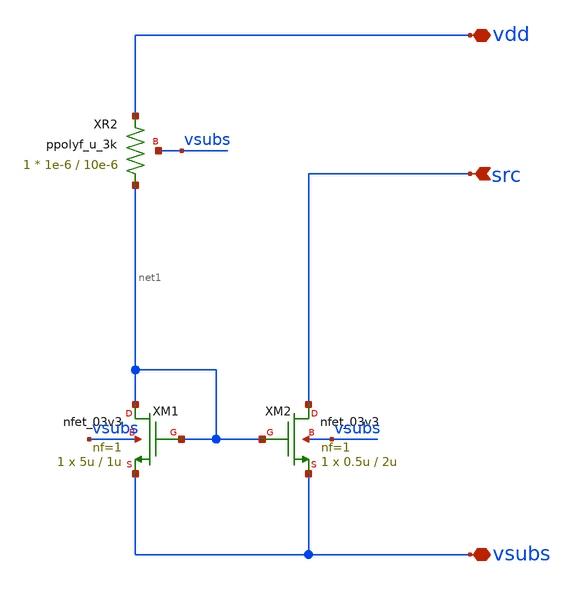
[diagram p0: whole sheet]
** sch_path: xschem/ip_current_source.sch
**.subckt ip_current_source vdd vsubs src
*.iopin vdd
*.iopin vsubs
*.ipin src
XM1 net1 net1 vsubs vsubs nfet_03v3 L=1u W=5u nf=1 ad='int((nf+1)/2) * W/nf * 0.18u' as='int((nf+2)/2) * W/nf * 0.18u'
+ pd='2*int((nf+1)/2) * (W/nf + 0.18u)' ps='2*int((nf+2)/2) * (W/nf + 0.18u)' nrd='0.18u / W' nrs='0.18u / W'
+ sa=0 sb=0 sd=0 m=1
XM2 src net1 vsubs vsubs nfet_03v3 L=2u W=0.5u nf=1 ad='int((nf+1)/2) * W/nf * 0.18u' as='int((nf+2)/2) * W/nf * 0.18u'
+ pd='2*int((nf+1)/2) * (W/nf + 0.18u)' ps='2*int((nf+2)/2) * (W/nf + 0.18u)' nrd='0.18u / W' nrs='0.18u / W'
+ sa=0 sb=0 sd=0 m=1
XR2 net1 vdd vsubs ppolyf_u_3k r_width=1e-6 r_length=10e-6 m=1
**.ends
.end
